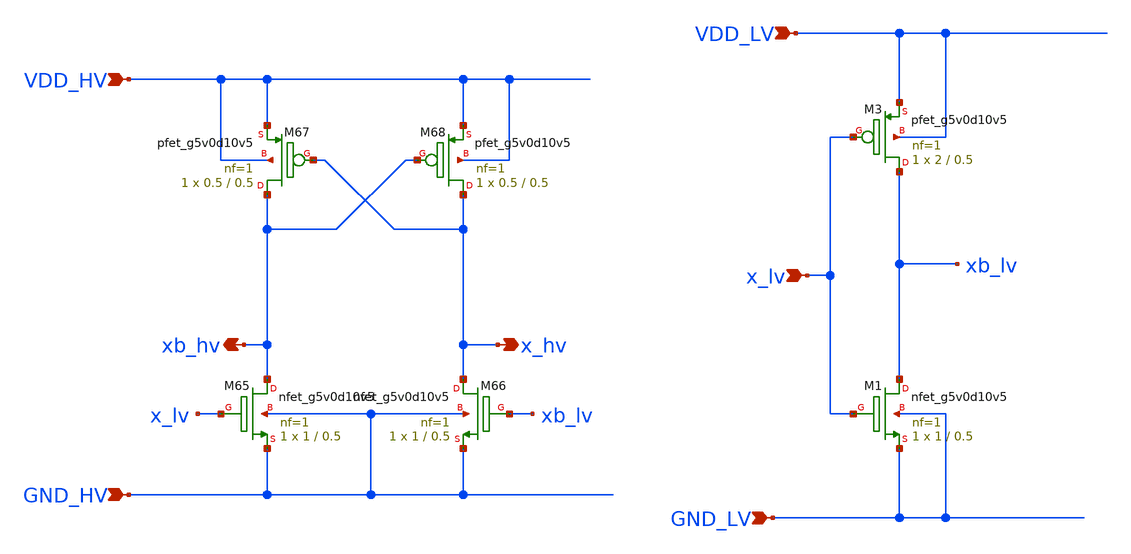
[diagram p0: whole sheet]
** sch_path: xschem/level_shifter_up.sch
**.subckt level_shifter_up VDD_HV GND_HV x_lv x_hv xb_hv VDD_LV GND_LV
*.ipin VDD_HV
*.ipin GND_HV
*.ipin x_lv
*.opin x_hv
*.opin xb_hv
*.ipin VDD_LV
*.ipin GND_LV
XM65 xb_hv x_lv GND_HV GND_HV sky130_fd_pr__nfet_g5v0d10v5 L=0.5 W=1 nf=1 ad='int((nf+1)/2) * W/nf * 0.29'
+ as='int((nf+2)/2) * W/nf * 0.29' pd='2*int((nf+1)/2) * (W/nf + 0.29)' ps='2*int((nf+2)/2) * (W/nf + 0.29)'
+ nrd='0.29 / W' nrs='0.29 / W' sa=0 sb=0 sd=0 mult=1 m=1
XM66 x_hv xb_lv GND_HV GND_HV sky130_fd_pr__nfet_g5v0d10v5 L=0.5 W=1 nf=1 ad='int((nf+1)/2) * W/nf * 0.29'
+ as='int((nf+2)/2) * W/nf * 0.29' pd='2*int((nf+1)/2) * (W/nf + 0.29)' ps='2*int((nf+2)/2) * (W/nf + 0.29)'
+ nrd='0.29 / W' nrs='0.29 / W' sa=0 sb=0 sd=0 mult=1 m=1
XM67 xb_hv x_hv VDD_HV VDD_HV sky130_fd_pr__pfet_g5v0d10v5 L=0.5 W=0.5 nf=1 ad='int((nf+1)/2) * W/nf * 0.29'
+ as='int((nf+2)/2) * W/nf * 0.29' pd='2*int((nf+1)/2) * (W/nf + 0.29)' ps='2*int((nf+2)/2) * (W/nf + 0.29)'
+ nrd='0.29 / W' nrs='0.29 / W' sa=0 sb=0 sd=0 mult=1 m=1
XM68 x_hv xb_hv VDD_HV VDD_HV sky130_fd_pr__pfet_g5v0d10v5 L=0.5 W=0.5 nf=1 ad='int((nf+1)/2) * W/nf * 0.29'
+ as='int((nf+2)/2) * W/nf * 0.29' pd='2*int((nf+1)/2) * (W/nf + 0.29)' ps='2*int((nf+2)/2) * (W/nf + 0.29)'
+ nrd='0.29 / W' nrs='0.29 / W' sa=0 sb=0 sd=0 mult=1 m=1
XM1 xb_lv x_lv GND_LV GND_LV sky130_fd_pr__nfet_g5v0d10v5 L=0.5 W=1 nf=1 ad='int((nf+1)/2) * W/nf * 0.29'
+ as='int((nf+2)/2) * W/nf * 0.29' pd='2*int((nf+1)/2) * (W/nf + 0.29)' ps='2*int((nf+2)/2) * (W/nf + 0.29)'
+ nrd='0.29 / W' nrs='0.29 / W' sa=0 sb=0 sd=0 mult=1 m=1
XM3 xb_lv x_lv VDD_LV VDD_LV sky130_fd_pr__pfet_g5v0d10v5 L=0.5 W=2 nf=1 ad='int((nf+1)/2) * W/nf * 0.29'
+ as='int((nf+2)/2) * W/nf * 0.29' pd='2*int((nf+1)/2) * (W/nf + 0.29)' ps='2*int((nf+2)/2) * (W/nf + 0.29)'
+ nrd='0.29 / W' nrs='0.29 / W' sa=0 sb=0 sd=0 mult=1 m=1
**.ends
.end
